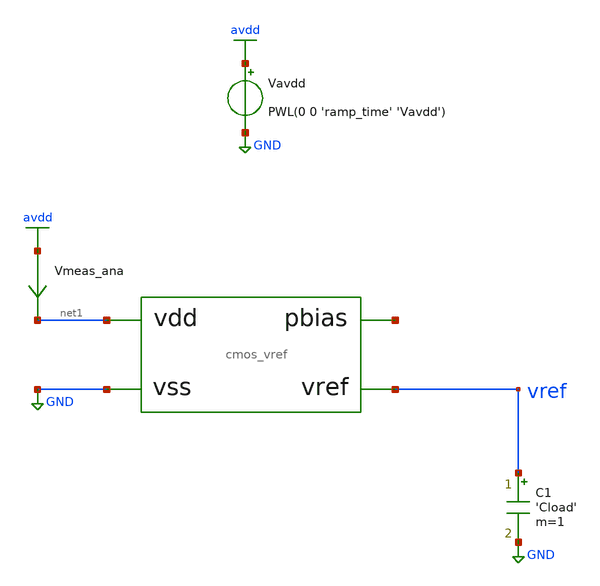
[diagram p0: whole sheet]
** sch_path: tb/cmos_vref/tb_vref_startup.sch
**.subckt tb_vref_startup
Vavdd avdd GND PWL(0 0 'ramp_time' 'Vavdd')
C1 vref GND 'Cload' m=1
Vmeas_ana avdd net1 0
.save i(vmeas_ana)
X1 vref net1 GND net2 cmos_vref
**** begin user architecture code


.lib 'models_dir'/cornerMOShv.lib 'mos_corner'
.lib 'models_dir'/cornerMOSlv.lib 'mos_corner'
.lib 'models_dir'/cornerCAP.lib cap_typ
.option TEMP='temperature'
.option warn=1
.control
save vref
tran 10n 1500u 0 100n
set wr_singlescale
wrdata 'simpath'/'filename'_'N'.data V(vref)
quit
.endc


**** end user architecture code
**.ends
.GLOBAL avdd
.GLOBAL GND
.end
